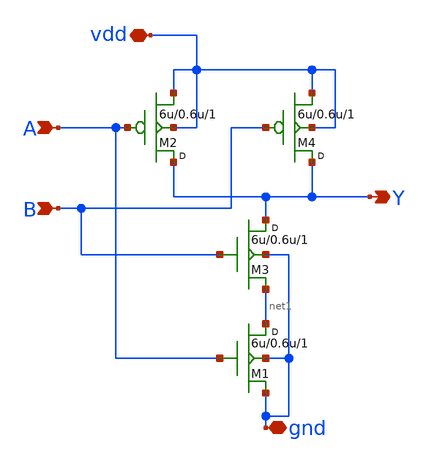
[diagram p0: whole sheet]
** sch_path: lab7/sch/made/NANDx.sch
**.subckt NANDx A B Y vdd gnd
*.ipin A
*.ipin B
*.opin Y
*.iopin vdd
*.iopin gnd
M3 Y B net1 gnd nfet w=6u l=0.6u m=1
M4 Y B vdd vdd pfet w=6u l=0.6u m=1
M2 Y A vdd vdd pfet w=6u l=0.6u m=1
M1 net1 A gnd gnd nfet w=6u l=0.6u m=1
**.ends
.end
